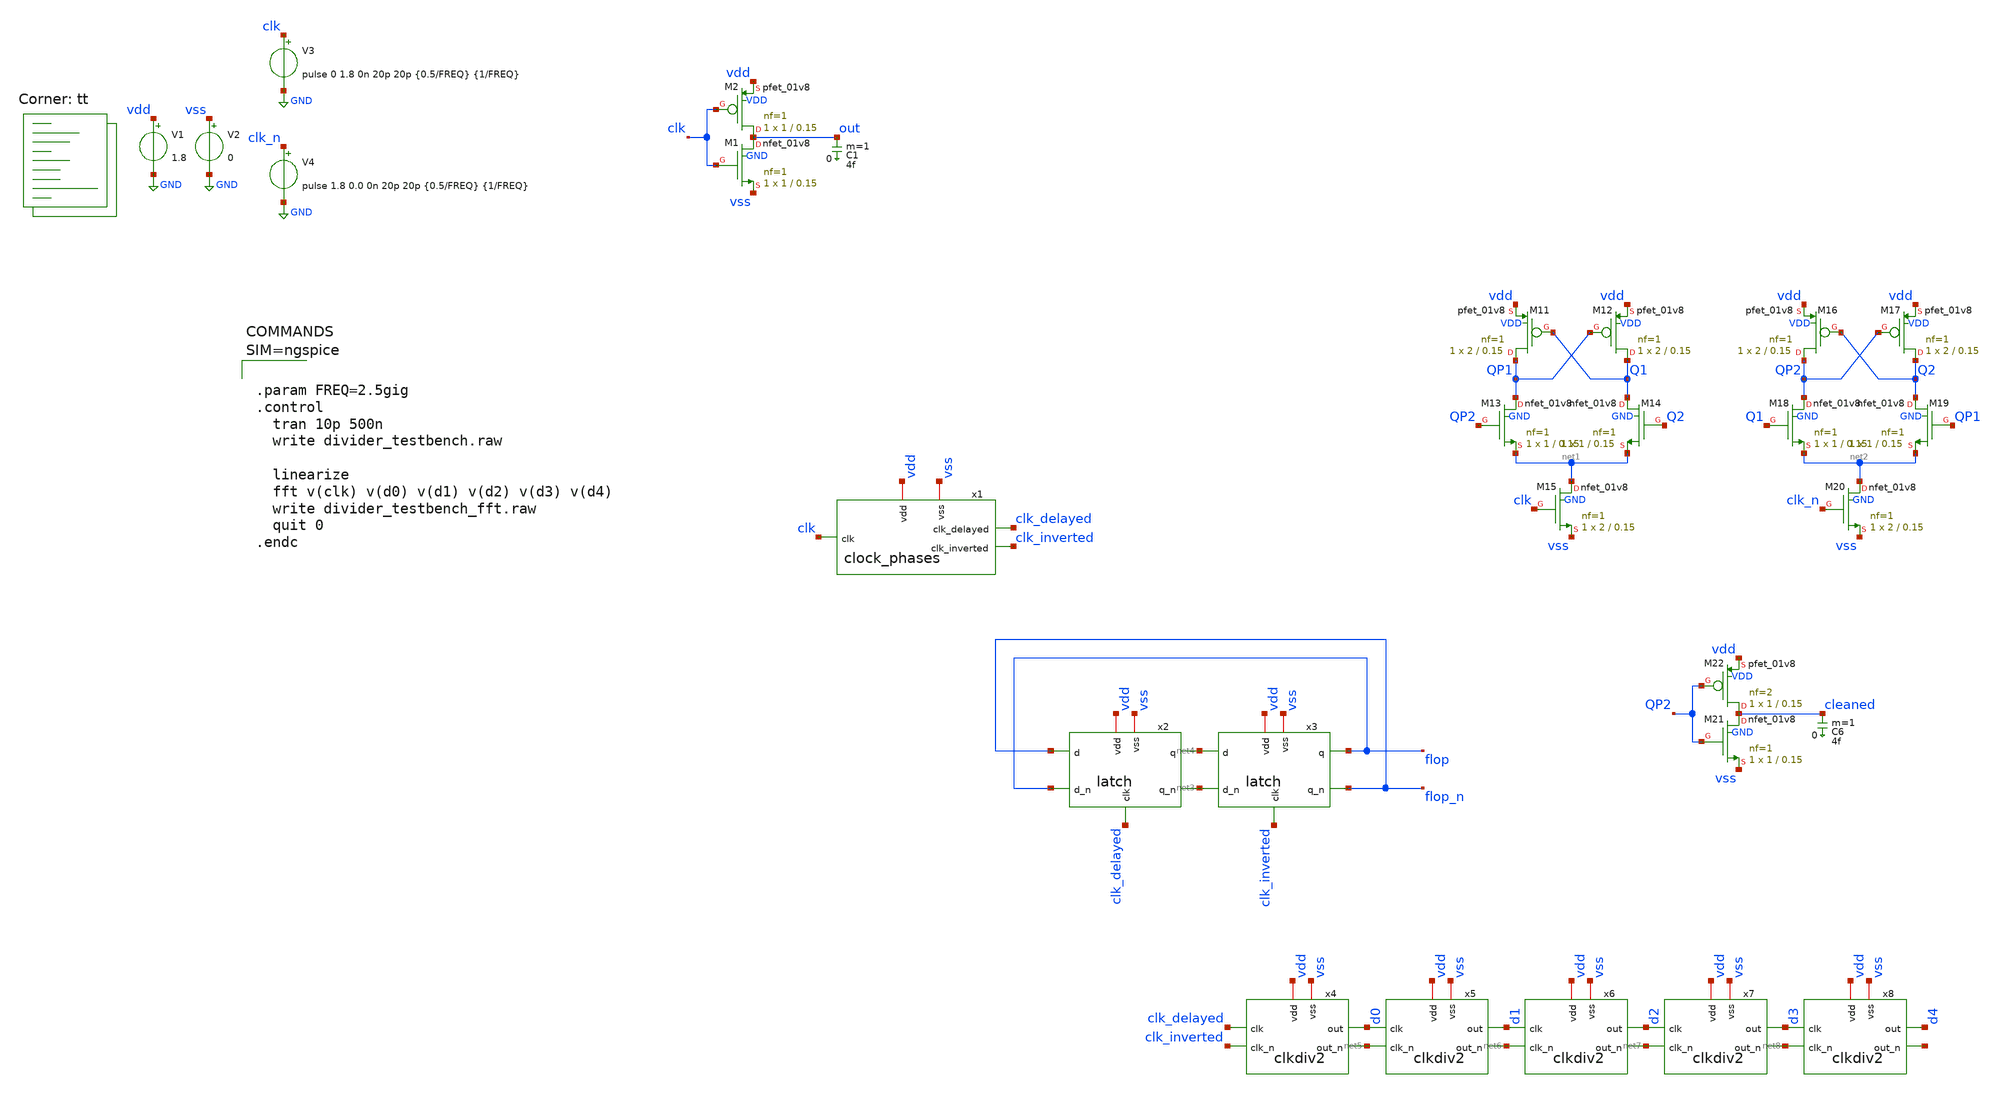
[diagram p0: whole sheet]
** sch_path: xschem/divider_testbench.sch
**.subckt divider_testbench
V1 vdd GND 1.8
V2 vss GND 0
V3 clk GND pulse 0 1.8 0n 20p 20p {0.5/FREQ} {1/FREQ}
XM1 out clk vss GND sky130_fd_pr__nfet_01v8 L=0.15 W=1 nf=1 ad='int((nf+1)/2) * W/nf * 0.29' as='int((nf+2)/2) * W/nf * 0.29'
+ pd='2*int((nf+1)/2) * (W/nf + 0.29)' ps='2*int((nf+2)/2) * (W/nf + 0.29)' nrd='0.29 / W' nrs='0.29 / W'
+ sa=0 sb=0 sd=0 mult=1 m=1
XM2 out clk vdd VDD sky130_fd_pr__pfet_01v8 L=0.15 W=1 nf=1 ad='int((nf+1)/2) * W/nf * 0.29' as='int((nf+2)/2) * W/nf * 0.29'
+ pd='2*int((nf+1)/2) * (W/nf + 0.29)' ps='2*int((nf+2)/2) * (W/nf + 0.29)' nrd='0.29 / W' nrs='0.29 / W'
+ sa=0 sb=0 sd=0 mult=1 m=1
C1 out 0 4f m=1
V4 clk_n GND pulse 1.8 0.0 0n 20p 20p {0.5/FREQ} {1/FREQ}
XM11 QP1 Q1 vdd VDD sky130_fd_pr__pfet_01v8 L=0.15 W=2 nf=1 ad='int((nf+1)/2) * W/nf * 0.29' as='int((nf+2)/2) * W/nf * 0.29'
+ pd='2*int((nf+1)/2) * (W/nf + 0.29)' ps='2*int((nf+2)/2) * (W/nf + 0.29)' nrd='0.29 / W' nrs='0.29 / W'
+ sa=0 sb=0 sd=0 mult=1 m=1
XM12 Q1 QP1 vdd VDD sky130_fd_pr__pfet_01v8 L=0.15 W=2 nf=1 ad='int((nf+1)/2) * W/nf * 0.29' as='int((nf+2)/2) * W/nf * 0.29'
+ pd='2*int((nf+1)/2) * (W/nf + 0.29)' ps='2*int((nf+2)/2) * (W/nf + 0.29)' nrd='0.29 / W' nrs='0.29 / W'
+ sa=0 sb=0 sd=0 mult=1 m=1
XM13 QP1 QP2 net1 GND sky130_fd_pr__nfet_01v8 L=0.15 W=1 nf=1 ad='int((nf+1)/2) * W/nf * 0.29' as='int((nf+2)/2) * W/nf * 0.29'
+ pd='2*int((nf+1)/2) * (W/nf + 0.29)' ps='2*int((nf+2)/2) * (W/nf + 0.29)' nrd='0.29 / W' nrs='0.29 / W'
+ sa=0 sb=0 sd=0 mult=1 m=1
XM14 Q1 Q2 net1 GND sky130_fd_pr__nfet_01v8 L=0.15 W=1 nf=1 ad='int((nf+1)/2) * W/nf * 0.29' as='int((nf+2)/2) * W/nf * 0.29'
+ pd='2*int((nf+1)/2) * (W/nf + 0.29)' ps='2*int((nf+2)/2) * (W/nf + 0.29)' nrd='0.29 / W' nrs='0.29 / W'
+ sa=0 sb=0 sd=0 mult=1 m=1
XM15 net1 clk vss GND sky130_fd_pr__nfet_01v8 L=0.15 W=2 nf=1 ad='int((nf+1)/2) * W/nf * 0.29' as='int((nf+2)/2) * W/nf * 0.29'
+ pd='2*int((nf+1)/2) * (W/nf + 0.29)' ps='2*int((nf+2)/2) * (W/nf + 0.29)' nrd='0.29 / W' nrs='0.29 / W'
+ sa=0 sb=0 sd=0 mult=1 m=1
XM16 QP2 Q2 vdd VDD sky130_fd_pr__pfet_01v8 L=0.15 W=2 nf=1 ad='int((nf+1)/2) * W/nf * 0.29' as='int((nf+2)/2) * W/nf * 0.29'
+ pd='2*int((nf+1)/2) * (W/nf + 0.29)' ps='2*int((nf+2)/2) * (W/nf + 0.29)' nrd='0.29 / W' nrs='0.29 / W'
+ sa=0 sb=0 sd=0 mult=1 m=1
XM17 Q2 QP2 vdd VDD sky130_fd_pr__pfet_01v8 L=0.15 W=2 nf=1 ad='int((nf+1)/2) * W/nf * 0.29' as='int((nf+2)/2) * W/nf * 0.29'
+ pd='2*int((nf+1)/2) * (W/nf + 0.29)' ps='2*int((nf+2)/2) * (W/nf + 0.29)' nrd='0.29 / W' nrs='0.29 / W'
+ sa=0 sb=0 sd=0 mult=1 m=1
XM18 QP2 Q1 net2 GND sky130_fd_pr__nfet_01v8 L=0.15 W=1 nf=1 ad='int((nf+1)/2) * W/nf * 0.29' as='int((nf+2)/2) * W/nf * 0.29'
+ pd='2*int((nf+1)/2) * (W/nf + 0.29)' ps='2*int((nf+2)/2) * (W/nf + 0.29)' nrd='0.29 / W' nrs='0.29 / W'
+ sa=0 sb=0 sd=0 mult=1 m=1
XM19 Q2 QP1 net2 GND sky130_fd_pr__nfet_01v8 L=0.15 W=1 nf=1 ad='int((nf+1)/2) * W/nf * 0.29' as='int((nf+2)/2) * W/nf * 0.29'
+ pd='2*int((nf+1)/2) * (W/nf + 0.29)' ps='2*int((nf+2)/2) * (W/nf + 0.29)' nrd='0.29 / W' nrs='0.29 / W'
+ sa=0 sb=0 sd=0 mult=1 m=1
XM20 net2 clk_n vss GND sky130_fd_pr__nfet_01v8 L=0.15 W=2 nf=1 ad='int((nf+1)/2) * W/nf * 0.29' as='int((nf+2)/2) * W/nf * 0.29'
+ pd='2*int((nf+1)/2) * (W/nf + 0.29)' ps='2*int((nf+2)/2) * (W/nf + 0.29)' nrd='0.29 / W' nrs='0.29 / W'
+ sa=0 sb=0 sd=0 mult=1 m=1
XM21 cleaned QP2 vss GND sky130_fd_pr__nfet_01v8 L=0.15 W=1 nf=1 ad='int((nf+1)/2) * W/nf * 0.29' as='int((nf+2)/2) * W/nf * 0.29'
+ pd='2*int((nf+1)/2) * (W/nf + 0.29)' ps='2*int((nf+2)/2) * (W/nf + 0.29)' nrd='0.29 / W' nrs='0.29 / W'
+ sa=0 sb=0 sd=0 mult=1 m=1
XM22 cleaned QP2 vdd VDD sky130_fd_pr__pfet_01v8 L=0.15 W=1 nf=2 ad='int((nf+1)/2) * W/nf * 0.29' as='int((nf+2)/2) * W/nf * 0.29'
+ pd='2*int((nf+1)/2) * (W/nf + 0.29)' ps='2*int((nf+2)/2) * (W/nf + 0.29)' nrd='0.29 / W' nrs='0.29 / W'
+ sa=0 sb=0 sd=0 mult=1 m=1
C6 cleaned 0 4f m=1
x1 vdd clk_delayed clk clk_inverted vss clock_phases
x2 vdd vss net3 net4 flop_n flop clk_delayed latch
x3 vdd vss flop_n flop net4 net3 clk_inverted latch
x4 vdd vss d0 net5 clk_inverted clk_delayed clkdiv2
x5 vdd vss d1 net6 net5 d0 clkdiv2
x6 vdd vss d2 net7 net6 d1 clkdiv2
x7 vdd vss d3 net8 net7 d2 clkdiv2
x8 vdd vss d4 net9 net8 d3 clkdiv2
**** begin user architecture code
.lib $::SKYWATER_MODELS/sky130.lib.spice tt



.param FREQ=2.5gig
.control
  tran 10p 500n
  write divider_testbench.raw

  linearize
  fft v(clk) v(d0) v(d1) v(d2) v(d3) v(d4)
  write divider_testbench_fft.raw
  quit 0
.endc



**** end user architecture code
**.ends

* expanding   symbol:  clock_phases.sym # of pins=5
** sym_path: xschem/clock_phases.sym
** sch_path: xschem/clock_phases.sch
.subckt clock_phases vdd clk_delayed clk clk_inverted vss
*.ipin clk
*.iopin vdd
*.opin clk_delayed
*.opin clk_inverted
*.iopin vss
XM3 net2 clk vss GND sky130_fd_pr__nfet_01v8 L=0.15 W=1 nf=1 ad='int((nf+1)/2) * W/nf * 0.29' as='int((nf+2)/2) * W/nf * 0.29'
+ pd='2*int((nf+1)/2) * (W/nf + 0.29)' ps='2*int((nf+2)/2) * (W/nf + 0.29)' nrd='0.29 / W' nrs='0.29 / W'
+ sa=0 sb=0 sd=0 mult=1 m=1
XM4 net2 clk vdd VDD sky130_fd_pr__pfet_01v8 L=0.15 W=1 nf=2 ad='int((nf+1)/2) * W/nf * 0.29' as='int((nf+2)/2) * W/nf * 0.29'
+ pd='2*int((nf+1)/2) * (W/nf + 0.29)' ps='2*int((nf+2)/2) * (W/nf + 0.29)' nrd='0.29 / W' nrs='0.29 / W'
+ sa=0 sb=0 sd=0 mult=1 m=1
XM5 net1 vdd clk GND sky130_fd_pr__nfet_01v8 L=0.15 W=1 nf=1 ad='int((nf+1)/2) * W/nf * 0.29' as='int((nf+2)/2) * W/nf * 0.29'
+ pd='2*int((nf+1)/2) * (W/nf + 0.29)' ps='2*int((nf+2)/2) * (W/nf + 0.29)' nrd='0.29 / W' nrs='0.29 / W'
+ sa=0 sb=0 sd=0 mult=1 m=1
XM6 net1 vss clk VDD sky130_fd_pr__pfet_01v8 L=0.15 W=1 nf=2 ad='int((nf+1)/2) * W/nf * 0.29' as='int((nf+2)/2) * W/nf * 0.29'
+ pd='2*int((nf+1)/2) * (W/nf + 0.29)' ps='2*int((nf+2)/2) * (W/nf + 0.29)' nrd='0.29 / W' nrs='0.29 / W'
+ sa=0 sb=0 sd=0 mult=1 m=1
XM7 clk_delayed net2 vss GND sky130_fd_pr__nfet_01v8 L=0.15 W=1 nf=1 ad='int((nf+1)/2) * W/nf * 0.29'
+ as='int((nf+2)/2) * W/nf * 0.29' pd='2*int((nf+1)/2) * (W/nf + 0.29)' ps='2*int((nf+2)/2) * (W/nf + 0.29)'
+ nrd='0.29 / W' nrs='0.29 / W' sa=0 sb=0 sd=0 mult=1 m=1
XM8 clk_delayed net2 vdd VDD sky130_fd_pr__pfet_01v8 L=0.15 W=1 nf=2 ad='int((nf+1)/2) * W/nf * 0.29'
+ as='int((nf+2)/2) * W/nf * 0.29' pd='2*int((nf+1)/2) * (W/nf + 0.29)' ps='2*int((nf+2)/2) * (W/nf + 0.29)'
+ nrd='0.29 / W' nrs='0.29 / W' sa=0 sb=0 sd=0 mult=1 m=1
XM9 clk_inverted net1 vss GND sky130_fd_pr__nfet_01v8 L=0.15 W=1 nf=1 ad='int((nf+1)/2) * W/nf * 0.29'
+ as='int((nf+2)/2) * W/nf * 0.29' pd='2*int((nf+1)/2) * (W/nf + 0.29)' ps='2*int((nf+2)/2) * (W/nf + 0.29)'
+ nrd='0.29 / W' nrs='0.29 / W' sa=0 sb=0 sd=0 mult=1 m=1
XM10 clk_inverted net1 vdd VDD sky130_fd_pr__pfet_01v8 L=0.15 W=1 nf=2 ad='int((nf+1)/2) * W/nf * 0.29'
+ as='int((nf+2)/2) * W/nf * 0.29' pd='2*int((nf+1)/2) * (W/nf + 0.29)' ps='2*int((nf+2)/2) * (W/nf + 0.29)'
+ nrd='0.29 / W' nrs='0.29 / W' sa=0 sb=0 sd=0 mult=1 m=1
.ends


* expanding   symbol:  latch.sym # of pins=7
** sym_path: xschem/latch.sym
** sch_path: xschem/latch.sch
.subckt latch vdd vss q_n q d d_n clk
*.iopin vdd
*.ipin d
*.opin q
*.iopin vss
*.ipin d_n
*.opin q_n
*.ipin clk
XM11 q_n q vdd vdd sky130_fd_pr__pfet_01v8 L=0.15 W=2 nf=1 ad='int((nf+1)/2) * W/nf * 0.29' as='int((nf+2)/2) * W/nf * 0.29'
+ pd='2*int((nf+1)/2) * (W/nf + 0.29)' ps='2*int((nf+2)/2) * (W/nf + 0.29)' nrd='0.29 / W' nrs='0.29 / W'
+ sa=0 sb=0 sd=0 mult=1 m=1
XM12 q q_n vdd vdd sky130_fd_pr__pfet_01v8 L=0.15 W=2 nf=1 ad='int((nf+1)/2) * W/nf * 0.29' as='int((nf+2)/2) * W/nf * 0.29'
+ pd='2*int((nf+1)/2) * (W/nf + 0.29)' ps='2*int((nf+2)/2) * (W/nf + 0.29)' nrd='0.29 / W' nrs='0.29 / W'
+ sa=0 sb=0 sd=0 mult=1 m=1
XM13 q_n d net1 vss sky130_fd_pr__nfet_01v8 L=0.15 W=1 nf=1 ad='int((nf+1)/2) * W/nf * 0.29' as='int((nf+2)/2) * W/nf * 0.29'
+ pd='2*int((nf+1)/2) * (W/nf + 0.29)' ps='2*int((nf+2)/2) * (W/nf + 0.29)' nrd='0.29 / W' nrs='0.29 / W'
+ sa=0 sb=0 sd=0 mult=1 m=1
XM14 q d_n net1 vss sky130_fd_pr__nfet_01v8 L=0.15 W=1 nf=1 ad='int((nf+1)/2) * W/nf * 0.29' as='int((nf+2)/2) * W/nf * 0.29'
+ pd='2*int((nf+1)/2) * (W/nf + 0.29)' ps='2*int((nf+2)/2) * (W/nf + 0.29)' nrd='0.29 / W' nrs='0.29 / W'
+ sa=0 sb=0 sd=0 mult=1 m=1
XM15 net1 clk vss vss sky130_fd_pr__nfet_01v8 L=0.15 W=2 nf=1 ad='int((nf+1)/2) * W/nf * 0.29' as='int((nf+2)/2) * W/nf * 0.29'
+ pd='2*int((nf+1)/2) * (W/nf + 0.29)' ps='2*int((nf+2)/2) * (W/nf + 0.29)' nrd='0.29 / W' nrs='0.29 / W'
+ sa=0 sb=0 sd=0 mult=1 m=1
.ends


* expanding   symbol:  clkdiv2.sym # of pins=6
** sym_path: xschem/clkdiv2.sym
** sch_path: xschem/clkdiv2.sch
.subckt clkdiv2 vdd vss out out_n clk_n clk
*.iopin vdd
*.opin out
*.iopin vss
*.ipin clk
*.opin out_n
*.ipin clk_n
x2 vdd vss net1 net2 out_n out clk latch
x3 vdd vss out_n out net2 net1 clk_n latch
.ends

.GLOBAL GND
.end
